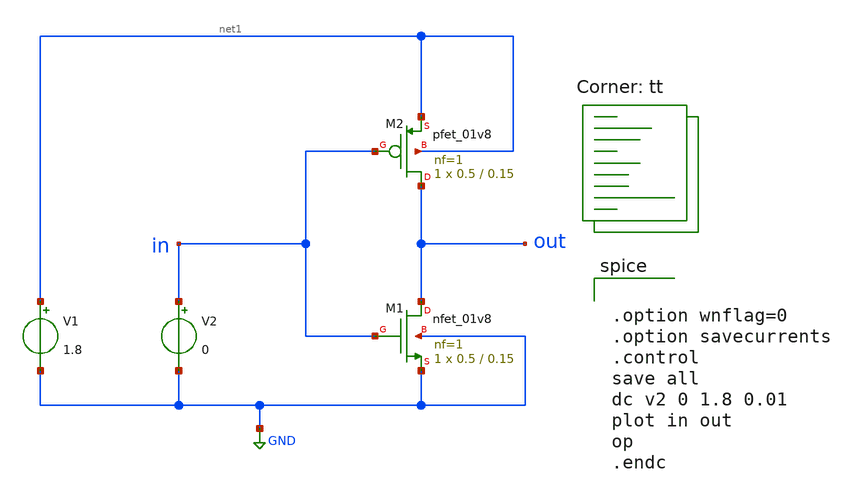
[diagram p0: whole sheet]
** sch_path: icdec_inverter2/inverter.sch
**.subckt inverter
XM1 out in GND GND sky130_fd_pr__nfet_01v8 L=0.15 W=0.5 nf=1 ad='int((nf+1)/2) * W/nf * 0.29' as='int((nf+2)/2) * W/nf * 0.29'
+ pd='2*int((nf+1)/2) * (W/nf + 0.29)' ps='2*int((nf+2)/2) * (W/nf + 0.29)' nrd='0.29 / W' nrs='0.29 / W'
+ sa=0 sb=0 sd=0 mult=1 m=1
XM2 out in net1 net1 sky130_fd_pr__pfet_01v8 L=0.15 W=0.5 nf=1 ad='int((nf+1)/2) * W/nf * 0.29' as='int((nf+2)/2) * W/nf * 0.29'
+ pd='2*int((nf+1)/2) * (W/nf + 0.29)' ps='2*int((nf+2)/2) * (W/nf + 0.29)' nrd='0.29 / W' nrs='0.29 / W'
+ sa=0 sb=0 sd=0 mult=1 m=1
V1 net1 GND 1.8
V2 in GND 0
**** begin user architecture code

** opencircuitdesign pdks install
.lib $::SKYWATER_MODELS/sky130.lib.spice tt




.option wnflag=0
.option savecurrents
.control
save all
dc v2 0 1.8 0.01
plot in out
op
.endc


**** end user architecture code
**.ends
.GLOBAL GND
.end
